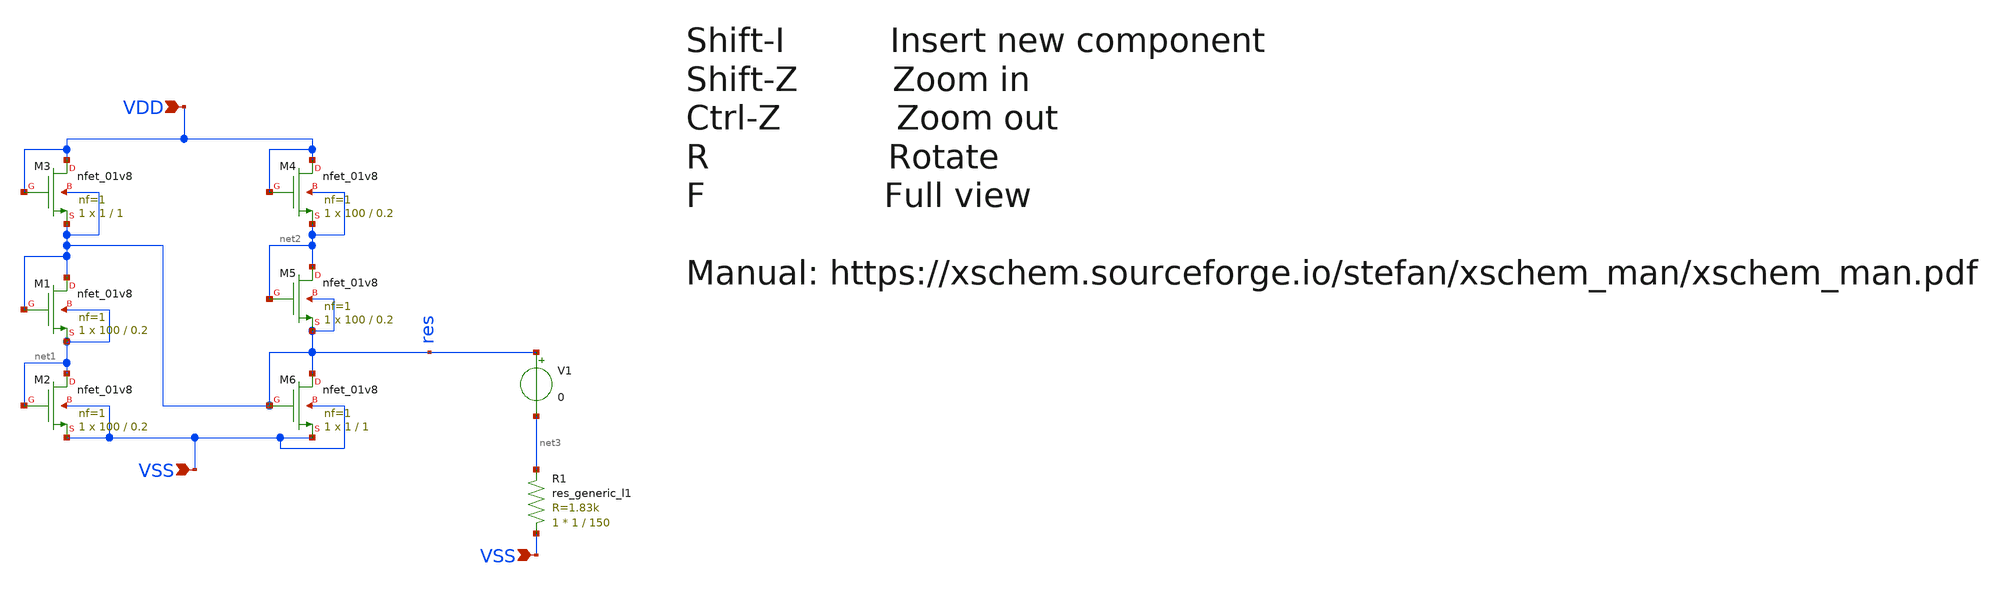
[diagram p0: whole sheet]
** sch_path: design/RPLY_EXTEMP0_SKY130NM/RPLY_EXTEMP0.sch
**.subckt RPLY_EXTEMP0 VDD VSS VSS
*.ipin VDD
*.ipin VSS
*.ipin VSS
XM1 res res net1 net1 sky130_fd_pr__nfet_01v8 L=0.2 W=100 nf=1 ad='int((nf+1)/2) * W/nf * 0.29' as='int((nf+2)/2) * W/nf * 0.29'
+ pd='2*int((nf+1)/2) * (W/nf + 0.29)' ps='2*int((nf+2)/2) * (W/nf + 0.29)' nrd='0.29 / W' nrs='0.29 / W'
+ sa=0 sb=0 sd=0 mult=1 m=1
XM2 net1 net1 VSS VSS sky130_fd_pr__nfet_01v8 L=0.2 W=100 nf=1 ad='int((nf+1)/2) * W/nf * 0.29' as='int((nf+2)/2) * W/nf * 0.29'
+ pd='2*int((nf+1)/2) * (W/nf + 0.29)' ps='2*int((nf+2)/2) * (W/nf + 0.29)' nrd='0.29 / W' nrs='0.29 / W'
+ sa=0 sb=0 sd=0 mult=1 m=1
XM3 VDD VDD res res sky130_fd_pr__nfet_01v8 L=1 W=1 nf=1 ad='int((nf+1)/2) * W/nf * 0.29' as='int((nf+2)/2) * W/nf * 0.29'
+ pd='2*int((nf+1)/2) * (W/nf + 0.29)' ps='2*int((nf+2)/2) * (W/nf + 0.29)' nrd='0.29 / W' nrs='0.29 / W'
+ sa=0 sb=0 sd=0 mult=1 m=1
XM4 VDD VDD net2 net2 sky130_fd_pr__nfet_01v8 L=0.2 W=100 nf=1 ad='int((nf+1)/2) * W/nf * 0.29' as='int((nf+2)/2) * W/nf * 0.29'
+ pd='2*int((nf+1)/2) * (W/nf + 0.29)' ps='2*int((nf+2)/2) * (W/nf + 0.29)' nrd='0.29 / W' nrs='0.29 / W'
+ sa=0 sb=0 sd=0 mult=1 m=1
XM5 net2 net2 res res sky130_fd_pr__nfet_01v8 L=0.2 W=100 nf=1 ad='int((nf+1)/2) * W/nf * 0.29' as='int((nf+2)/2) * W/nf * 0.29'
+ pd='2*int((nf+1)/2) * (W/nf + 0.29)' ps='2*int((nf+2)/2) * (W/nf + 0.29)' nrd='0.29 / W' nrs='0.29 / W'
+ sa=0 sb=0 sd=0 mult=1 m=1
XM6 res res VSS VSS sky130_fd_pr__nfet_01v8 L=1 W=1 nf=1 ad='int((nf+1)/2) * W/nf * 0.29' as='int((nf+2)/2) * W/nf * 0.29'
+ pd='2*int((nf+1)/2) * (W/nf + 0.29)' ps='2*int((nf+2)/2) * (W/nf + 0.29)' nrd='0.29 / W' nrs='0.29 / W'
+ sa=0 sb=0 sd=0 mult=1 m=1
V1 res net3 0
R1 VSS net3 sky130_fd_pr__res_generic_l1 W=1 L=150 m=1
**.ends
.end
